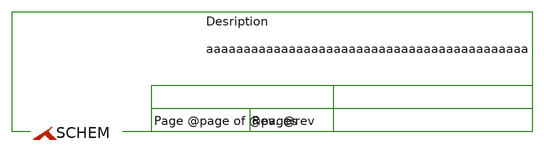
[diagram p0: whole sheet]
** sch_path: .config/xschem/template.sch
* Copyright (C) 1998-2024 Stefan Frederik Schippers
* This program is free software; you can redistribute it and/or modify
* it under the terms of the GNU General Public License as published by
* the Free Software Foundation; either version 2 of the License, or
* (at your option) any later version.
* This program is distributed in the hope that it will be useful,
* but WITHOUT ANY WARRANTY; without even the implied warranty of
* MERCHANTABILITY or FITNESS FOR A PARTICULAR PURPOSE.  See the
* GNU General Public License for more details.
* You should have received a copy of the GNU General Public License
* along with this program; if not, write to the Free Software
**.subckt template
**** begin user architecture code


.lib cornerMOSlv.lib mos_tt
.lib cornerMOShv.lib mos_tt
.lib cornerRES.lib res_typ
.include /home/vasil/CAD_VLSI/IHP-Open-PDK/ihp-sg13g2/libs.ref/sg13g2_stdcell/spice/sg13g2_stdcell.spice




.temp 27
.param vin=0


**** end user architecture code
**.ends
.end
